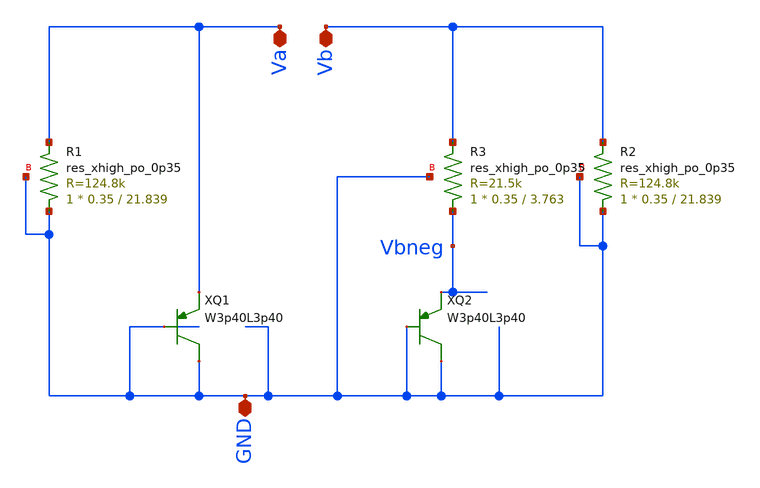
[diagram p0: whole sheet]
** sch_path: schematics/bandgapCore.sch
**.subckt bandgapCore Va Vb GND
*.iopin Va
*.iopin Vb
*.iopin GND
XR1 GND Va GND sky130_fd_pr__res_xhigh_po_0p35 L=21.839 mult=1 m=1
XR2 GND Vb GND sky130_fd_pr__res_xhigh_po_0p35 L=21.839 mult=1 m=1
XR3 Vbneg Vb GND sky130_fd_pr__res_xhigh_po_0p35 L=3.763 mult=1 m=1
XQ1 GND GND Va sky130_fd_pr__pnp_05v5 m=1
XQ2 GND GND Vbneg sky130_fd_pr__pnp_05v5 m=39
**.ends
.end
